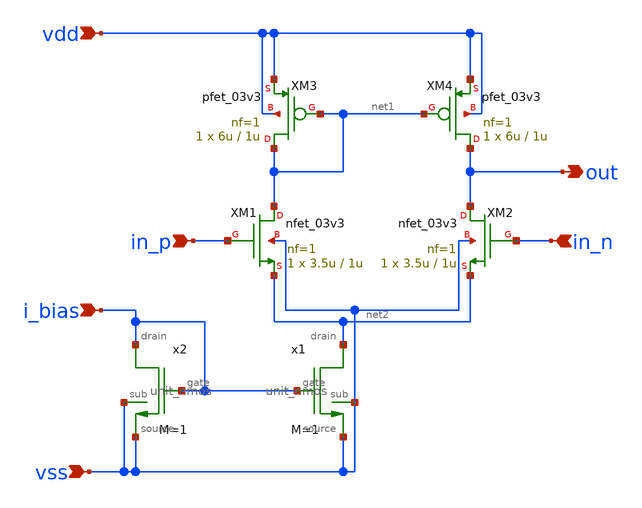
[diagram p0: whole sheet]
** sch_path: designs/switch_matrix_gf180mcu_9t5v0-main/designs/libs/core_analog/ota_5t/ota_5t.sch
**.subckt ota_5t in_p in_n i_bias vdd vss out
*.ipin in_p
*.ipin in_n
*.ipin i_bias
*.ipin vdd
*.ipin vss
*.opin out
XM1 net1 in_p net2 vss nfet_03v3 L=1u W=3.5u nf=1 ad='int((nf+1)/2) * W/nf * 0.18u' as='int((nf+2)/2) * W/nf * 0.18u'
+ pd='2*int((nf+1)/2) * (W/nf + 0.18u)' ps='2*int((nf+2)/2) * (W/nf + 0.18u)' nrd='0.18u / W' nrs='0.18u / W'
+ sa=0 sb=0 sd=0 m=1
XM2 out in_n net2 vss nfet_03v3 L=1u W=3.5u nf=1 ad='int((nf+1)/2) * W/nf * 0.18u' as='int((nf+2)/2) * W/nf * 0.18u'
+ pd='2*int((nf+1)/2) * (W/nf + 0.18u)' ps='2*int((nf+2)/2) * (W/nf + 0.18u)' nrd='0.18u / W' nrs='0.18u / W'
+ sa=0 sb=0 sd=0 m=1
XM4 out net1 vdd vdd pfet_03v3 L=1u W=6u nf=1 ad='int((nf+1)/2) * W/nf * 0.18u' as='int((nf+2)/2) * W/nf * 0.18u'
+ pd='2*int((nf+1)/2) * (W/nf + 0.18u)' ps='2*int((nf+2)/2) * (W/nf + 0.18u)' nrd='0.18u / W' nrs='0.18u / W'
+ sa=0 sb=0 sd=0 m=1
XM3 net1 net1 vdd vdd pfet_03v3 L=1u W=6u nf=1 ad='int((nf+1)/2) * W/nf * 0.18u' as='int((nf+2)/2) * W/nf * 0.18u'
+ pd='2*int((nf+1)/2) * (W/nf + 0.18u)' ps='2*int((nf+2)/2) * (W/nf + 0.18u)' nrd='0.18u / W' nrs='0.18u / W'
+ sa=0 sb=0 sd=0 m=1
x1 net2 vss i_bias vss unit_nmos M=1
x2 i_bias vss i_bias vss unit_nmos M=1
**.ends
.end
